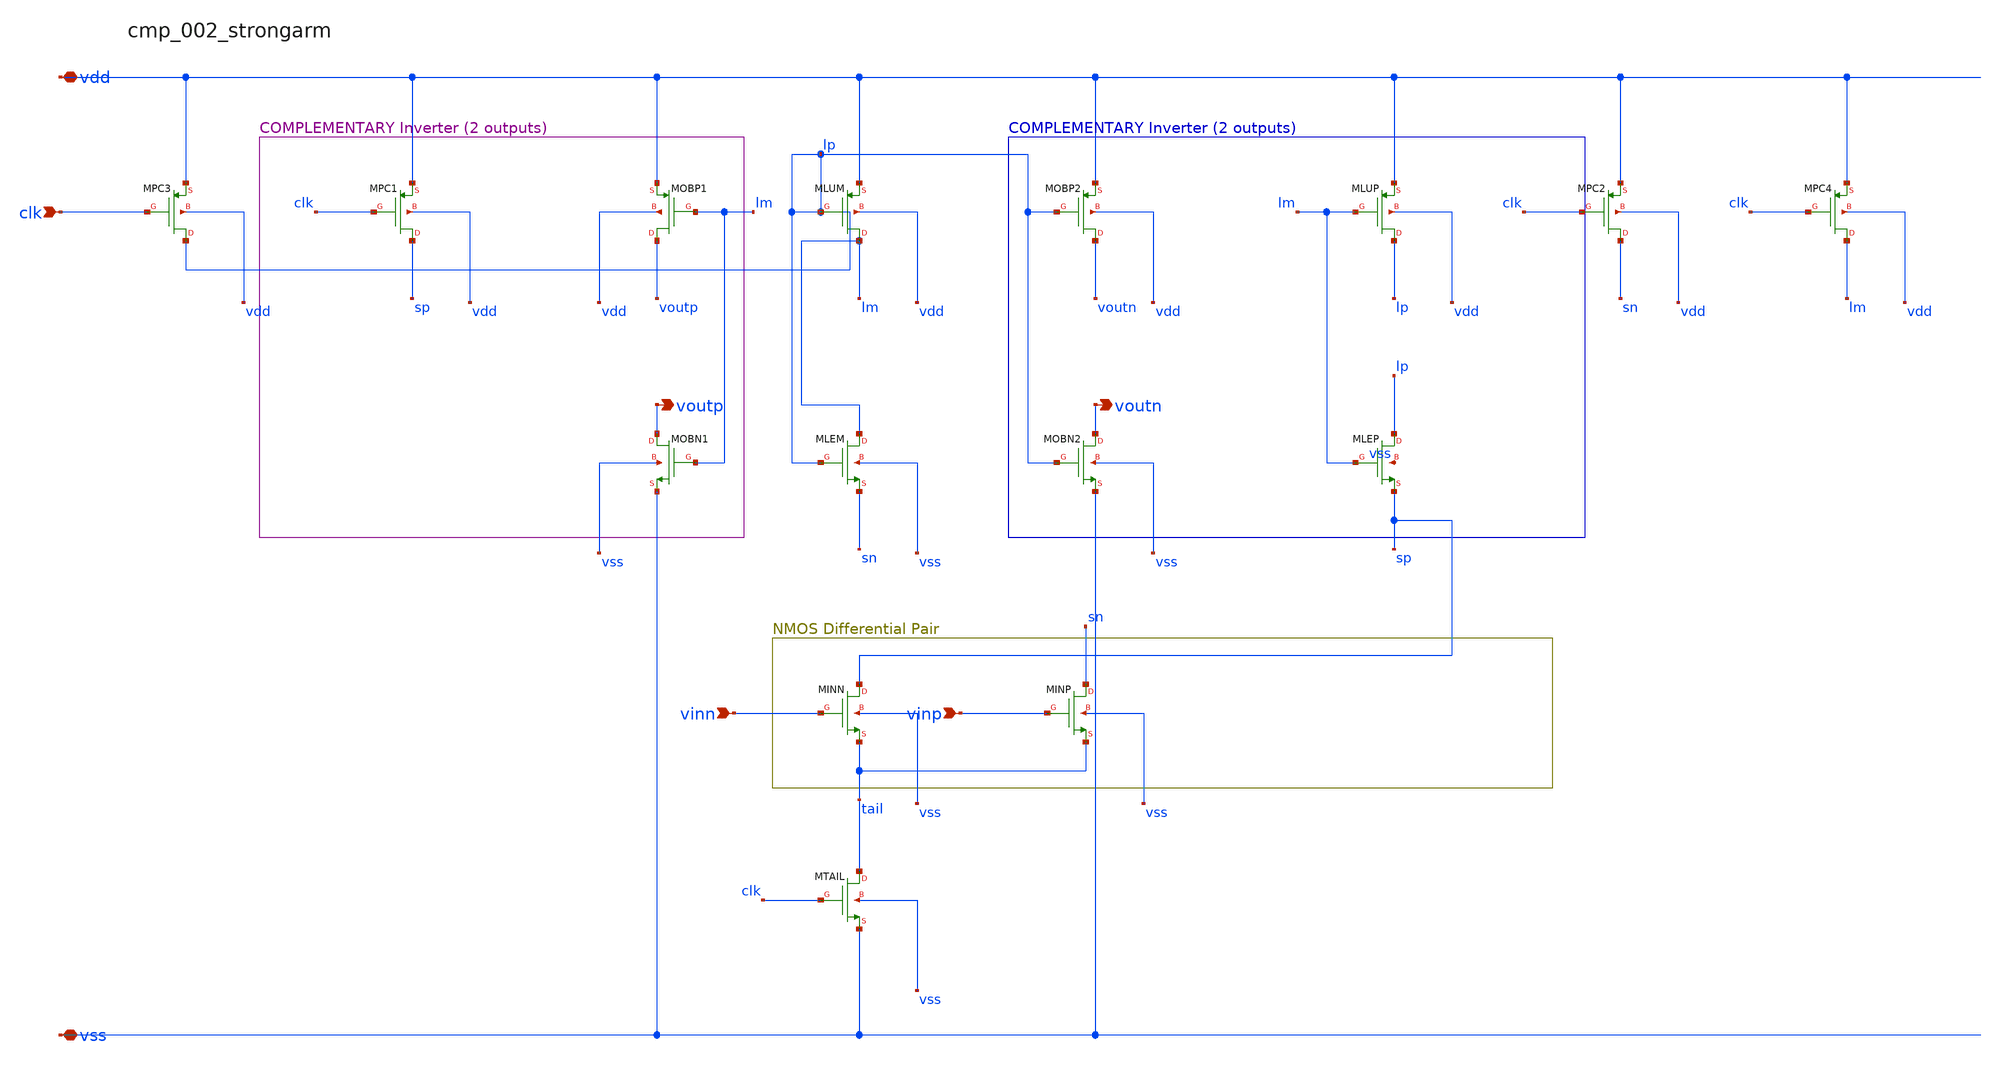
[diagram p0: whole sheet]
** sch_path: analog-db/raw/cmp_002_strongarm/cmp_002_strongarm_annotated.sch
**.subckt cmp_002_strongarm_annotated clk vinn vinp vdd vss voutp voutn
*.ipin clk
*.ipin vinn
*.ipin vinp
*.iopin vdd
*.iopin vss
*.opin voutp
*.opin voutn
XMINN sp vinn tail vss sg13_lv_nmos w=x_dut_xminn_w l=x_dut_xminn_l ng=1 m=x_dut_xminn_m
XMINP sn vinp tail vss sg13_lv_nmos w=x_dut_xminp_w l=x_dut_xminp_l ng=1 m=x_dut_xminp_m
XMLEM lm lp sn vss sg13_lv_nmos w=x_dut_xmlem_w l=x_dut_xmlem_l ng=1 m=x_dut_xmlem_m
XMLEP lp lm sp vss sg13_lv_nmos w=x_dut_xmlep_w l=x_dut_xmlep_l ng=1 m=x_dut_xmlep_m
XMLUM lm lp vdd vdd sg13_lv_pmos w=x_dut_xmlum_w l=x_dut_xmlum_l ng=1 m=x_dut_xmlum_m
XMLUP lp lm vdd vdd sg13_lv_pmos w=x_dut_xmlup_w l=x_dut_xmlup_l ng=1 m=x_dut_xmlup_m
XMOBN1 voutp lm vss vss sg13_lv_nmos w=x_dut_xmobn1_w l=x_dut_xmobn1_l ng=1 m=x_dut_xmobn1_m
XMOBN2 voutn lp vss vss sg13_lv_nmos w=x_dut_xmobn2_w l=x_dut_xmobn2_l ng=1 m=x_dut_xmobn2_m
XMOBP1 voutp lm vdd vdd sg13_lv_pmos w=x_dut_xmobp1_w l=x_dut_xmobp1_l ng=1 m=x_dut_xmobp1_m
XMOBP2 voutn lp vdd vdd sg13_lv_pmos w=x_dut_xmobp2_w l=x_dut_xmobp2_l ng=1 m=x_dut_xmobp2_m
XMPC1 sp clk vdd vdd sg13_lv_pmos w=x_dut_xmpc1_w l=x_dut_xmpc1_l ng=1 m=x_dut_xmpc1_m
XMPC2 sn clk vdd vdd sg13_lv_pmos w=x_dut_xmpc2_w l=x_dut_xmpc2_l ng=1 m=x_dut_xmpc2_m
XMPC3 lp clk vdd vdd sg13_lv_pmos w=x_dut_xmpc3_w l=x_dut_xmpc3_l ng=1 m=x_dut_xmpc3_m
XMPC4 lm clk vdd vdd sg13_lv_pmos w=x_dut_xmpc4_w l=x_dut_xmpc4_l ng=1 m=x_dut_xmpc4_m
XMTAIL tail clk vss vss sg13_lv_nmos w=x_dut_xmtail_w l=x_dut_xmtail_l ng=1 m=x_dut_xmtail_m
**.ends
.end
